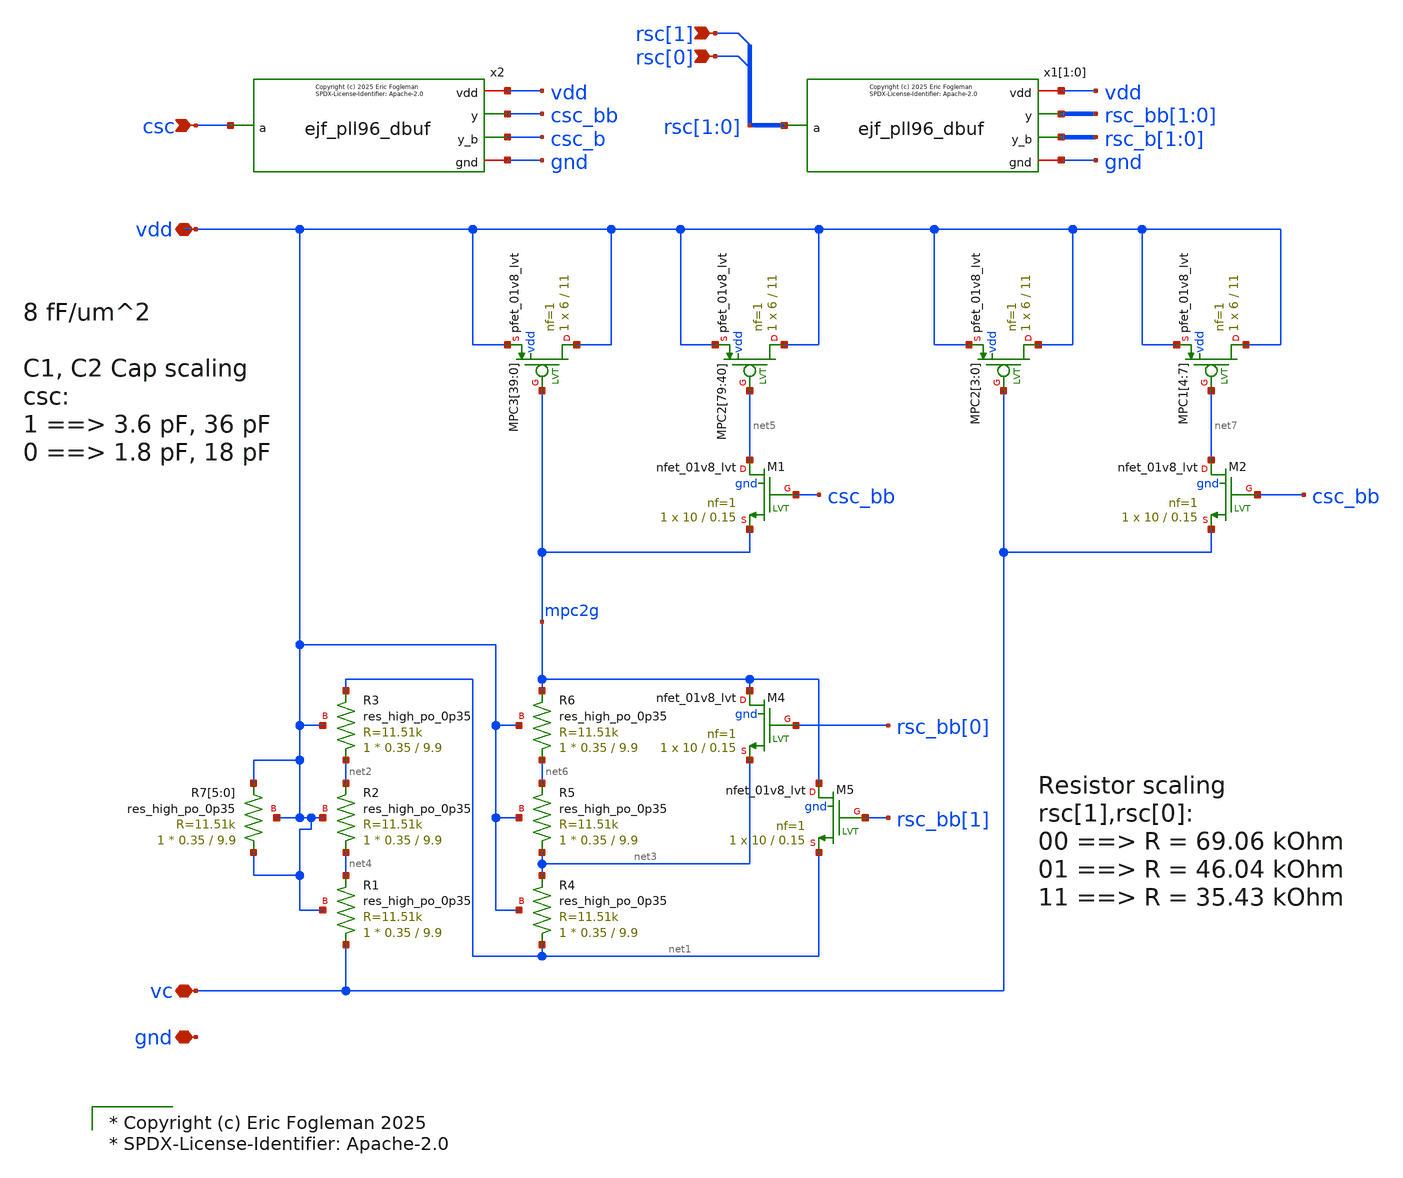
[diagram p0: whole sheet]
** sch_path: xschem/ejf_pll96_lpf.sch
* xschem/ejf_pll96_dbuf.sym:
* Copyright (c) 2025 Eric Fogleman

* Copyright (c) Eric Fogleman 2025
* SPDX-License-Identifier: Apache-2.0

**.subckt ejf_pll96_lpf vc vdd gnd csc rsc[0] rsc[1]
*.iopin vc
*.iopin vdd
*.iopin gnd
*.ipin csc
*.ipin rsc[0]
*.ipin rsc[1]
XMPC2[3] vdd vc vdd vdd sky130_fd_pr__pfet_01v8_lvt L=11 W=6 nf=1 ad='int((nf+1)/2) * W/nf * 0.29' as='int((nf+2)/2) * W/nf * 0.29'
+ pd='2*int((nf+1)/2) * (W/nf + 0.29)' ps='2*int((nf+2)/2) * (W/nf + 0.29)' nrd='0.29 / W' nrs='0.29 / W'
+ sa=0 sb=0 sd=0 mult=1 m=1
XMPC2[2] vdd vc vdd vdd sky130_fd_pr__pfet_01v8_lvt L=11 W=6 nf=1 ad='int((nf+1)/2) * W/nf * 0.29' as='int((nf+2)/2) * W/nf * 0.29'
+ pd='2*int((nf+1)/2) * (W/nf + 0.29)' ps='2*int((nf+2)/2) * (W/nf + 0.29)' nrd='0.29 / W' nrs='0.29 / W'
+ sa=0 sb=0 sd=0 mult=1 m=1
XMPC2[1] vdd vc vdd vdd sky130_fd_pr__pfet_01v8_lvt L=11 W=6 nf=1 ad='int((nf+1)/2) * W/nf * 0.29' as='int((nf+2)/2) * W/nf * 0.29'
+ pd='2*int((nf+1)/2) * (W/nf + 0.29)' ps='2*int((nf+2)/2) * (W/nf + 0.29)' nrd='0.29 / W' nrs='0.29 / W'
+ sa=0 sb=0 sd=0 mult=1 m=1
XMPC2[0] vdd vc vdd vdd sky130_fd_pr__pfet_01v8_lvt L=11 W=6 nf=1 ad='int((nf+1)/2) * W/nf * 0.29' as='int((nf+2)/2) * W/nf * 0.29'
+ pd='2*int((nf+1)/2) * (W/nf + 0.29)' ps='2*int((nf+2)/2) * (W/nf + 0.29)' nrd='0.29 / W' nrs='0.29 / W'
+ sa=0 sb=0 sd=0 mult=1 m=1
XMPC2[79] vdd net5 vdd vdd sky130_fd_pr__pfet_01v8_lvt L=11 W=6 nf=1 ad='int((nf+1)/2) * W/nf * 0.29'
+ as='int((nf+2)/2) * W/nf * 0.29' pd='2*int((nf+1)/2) * (W/nf + 0.29)' ps='2*int((nf+2)/2) * (W/nf + 0.29)'
+ nrd='0.29 / W' nrs='0.29 / W' sa=0 sb=0 sd=0 mult=1 m=1
XMPC2[78] vdd net5 vdd vdd sky130_fd_pr__pfet_01v8_lvt L=11 W=6 nf=1 ad='int((nf+1)/2) * W/nf * 0.29'
+ as='int((nf+2)/2) * W/nf * 0.29' pd='2*int((nf+1)/2) * (W/nf + 0.29)' ps='2*int((nf+2)/2) * (W/nf + 0.29)'
+ nrd='0.29 / W' nrs='0.29 / W' sa=0 sb=0 sd=0 mult=1 m=1
XMPC2[77] vdd net5 vdd vdd sky130_fd_pr__pfet_01v8_lvt L=11 W=6 nf=1 ad='int((nf+1)/2) * W/nf * 0.29'
+ as='int((nf+2)/2) * W/nf * 0.29' pd='2*int((nf+1)/2) * (W/nf + 0.29)' ps='2*int((nf+2)/2) * (W/nf + 0.29)'
+ nrd='0.29 / W' nrs='0.29 / W' sa=0 sb=0 sd=0 mult=1 m=1
XMPC2[76] vdd net5 vdd vdd sky130_fd_pr__pfet_01v8_lvt L=11 W=6 nf=1 ad='int((nf+1)/2) * W/nf * 0.29'
+ as='int((nf+2)/2) * W/nf * 0.29' pd='2*int((nf+1)/2) * (W/nf + 0.29)' ps='2*int((nf+2)/2) * (W/nf + 0.29)'
+ nrd='0.29 / W' nrs='0.29 / W' sa=0 sb=0 sd=0 mult=1 m=1
XMPC2[75] vdd net5 vdd vdd sky130_fd_pr__pfet_01v8_lvt L=11 W=6 nf=1 ad='int((nf+1)/2) * W/nf * 0.29'
+ as='int((nf+2)/2) * W/nf * 0.29' pd='2*int((nf+1)/2) * (W/nf + 0.29)' ps='2*int((nf+2)/2) * (W/nf + 0.29)'
+ nrd='0.29 / W' nrs='0.29 / W' sa=0 sb=0 sd=0 mult=1 m=1
XMPC2[74] vdd net5 vdd vdd sky130_fd_pr__pfet_01v8_lvt L=11 W=6 nf=1 ad='int((nf+1)/2) * W/nf * 0.29'
+ as='int((nf+2)/2) * W/nf * 0.29' pd='2*int((nf+1)/2) * (W/nf + 0.29)' ps='2*int((nf+2)/2) * (W/nf + 0.29)'
+ nrd='0.29 / W' nrs='0.29 / W' sa=0 sb=0 sd=0 mult=1 m=1
XMPC2[73] vdd net5 vdd vdd sky130_fd_pr__pfet_01v8_lvt L=11 W=6 nf=1 ad='int((nf+1)/2) * W/nf * 0.29'
+ as='int((nf+2)/2) * W/nf * 0.29' pd='2*int((nf+1)/2) * (W/nf + 0.29)' ps='2*int((nf+2)/2) * (W/nf + 0.29)'
+ nrd='0.29 / W' nrs='0.29 / W' sa=0 sb=0 sd=0 mult=1 m=1
XMPC2[72] vdd net5 vdd vdd sky130_fd_pr__pfet_01v8_lvt L=11 W=6 nf=1 ad='int((nf+1)/2) * W/nf * 0.29'
+ as='int((nf+2)/2) * W/nf * 0.29' pd='2*int((nf+1)/2) * (W/nf + 0.29)' ps='2*int((nf+2)/2) * (W/nf + 0.29)'
+ nrd='0.29 / W' nrs='0.29 / W' sa=0 sb=0 sd=0 mult=1 m=1
XMPC2[71] vdd net5 vdd vdd sky130_fd_pr__pfet_01v8_lvt L=11 W=6 nf=1 ad='int((nf+1)/2) * W/nf * 0.29'
+ as='int((nf+2)/2) * W/nf * 0.29' pd='2*int((nf+1)/2) * (W/nf + 0.29)' ps='2*int((nf+2)/2) * (W/nf + 0.29)'
+ nrd='0.29 / W' nrs='0.29 / W' sa=0 sb=0 sd=0 mult=1 m=1
XMPC2[70] vdd net5 vdd vdd sky130_fd_pr__pfet_01v8_lvt L=11 W=6 nf=1 ad='int((nf+1)/2) * W/nf * 0.29'
+ as='int((nf+2)/2) * W/nf * 0.29' pd='2*int((nf+1)/2) * (W/nf + 0.29)' ps='2*int((nf+2)/2) * (W/nf + 0.29)'
+ nrd='0.29 / W' nrs='0.29 / W' sa=0 sb=0 sd=0 mult=1 m=1
XMPC2[69] vdd net5 vdd vdd sky130_fd_pr__pfet_01v8_lvt L=11 W=6 nf=1 ad='int((nf+1)/2) * W/nf * 0.29'
+ as='int((nf+2)/2) * W/nf * 0.29' pd='2*int((nf+1)/2) * (W/nf + 0.29)' ps='2*int((nf+2)/2) * (W/nf + 0.29)'
+ nrd='0.29 / W' nrs='0.29 / W' sa=0 sb=0 sd=0 mult=1 m=1
XMPC2[68] vdd net5 vdd vdd sky130_fd_pr__pfet_01v8_lvt L=11 W=6 nf=1 ad='int((nf+1)/2) * W/nf * 0.29'
+ as='int((nf+2)/2) * W/nf * 0.29' pd='2*int((nf+1)/2) * (W/nf + 0.29)' ps='2*int((nf+2)/2) * (W/nf + 0.29)'
+ nrd='0.29 / W' nrs='0.29 / W' sa=0 sb=0 sd=0 mult=1 m=1
XMPC2[67] vdd net5 vdd vdd sky130_fd_pr__pfet_01v8_lvt L=11 W=6 nf=1 ad='int((nf+1)/2) * W/nf * 0.29'
+ as='int((nf+2)/2) * W/nf * 0.29' pd='2*int((nf+1)/2) * (W/nf + 0.29)' ps='2*int((nf+2)/2) * (W/nf + 0.29)'
+ nrd='0.29 / W' nrs='0.29 / W' sa=0 sb=0 sd=0 mult=1 m=1
XMPC2[66] vdd net5 vdd vdd sky130_fd_pr__pfet_01v8_lvt L=11 W=6 nf=1 ad='int((nf+1)/2) * W/nf * 0.29'
+ as='int((nf+2)/2) * W/nf * 0.29' pd='2*int((nf+1)/2) * (W/nf + 0.29)' ps='2*int((nf+2)/2) * (W/nf + 0.29)'
+ nrd='0.29 / W' nrs='0.29 / W' sa=0 sb=0 sd=0 mult=1 m=1
XMPC2[65] vdd net5 vdd vdd sky130_fd_pr__pfet_01v8_lvt L=11 W=6 nf=1 ad='int((nf+1)/2) * W/nf * 0.29'
+ as='int((nf+2)/2) * W/nf * 0.29' pd='2*int((nf+1)/2) * (W/nf + 0.29)' ps='2*int((nf+2)/2) * (W/nf + 0.29)'
+ nrd='0.29 / W' nrs='0.29 / W' sa=0 sb=0 sd=0 mult=1 m=1
XMPC2[64] vdd net5 vdd vdd sky130_fd_pr__pfet_01v8_lvt L=11 W=6 nf=1 ad='int((nf+1)/2) * W/nf * 0.29'
+ as='int((nf+2)/2) * W/nf * 0.29' pd='2*int((nf+1)/2) * (W/nf + 0.29)' ps='2*int((nf+2)/2) * (W/nf + 0.29)'
+ nrd='0.29 / W' nrs='0.29 / W' sa=0 sb=0 sd=0 mult=1 m=1
XMPC2[63] vdd net5 vdd vdd sky130_fd_pr__pfet_01v8_lvt L=11 W=6 nf=1 ad='int((nf+1)/2) * W/nf * 0.29'
+ as='int((nf+2)/2) * W/nf * 0.29' pd='2*int((nf+1)/2) * (W/nf + 0.29)' ps='2*int((nf+2)/2) * (W/nf + 0.29)'
+ nrd='0.29 / W' nrs='0.29 / W' sa=0 sb=0 sd=0 mult=1 m=1
XMPC2[62] vdd net5 vdd vdd sky130_fd_pr__pfet_01v8_lvt L=11 W=6 nf=1 ad='int((nf+1)/2) * W/nf * 0.29'
+ as='int((nf+2)/2) * W/nf * 0.29' pd='2*int((nf+1)/2) * (W/nf + 0.29)' ps='2*int((nf+2)/2) * (W/nf + 0.29)'
+ nrd='0.29 / W' nrs='0.29 / W' sa=0 sb=0 sd=0 mult=1 m=1
XMPC2[61] vdd net5 vdd vdd sky130_fd_pr__pfet_01v8_lvt L=11 W=6 nf=1 ad='int((nf+1)/2) * W/nf * 0.29'
+ as='int((nf+2)/2) * W/nf * 0.29' pd='2*int((nf+1)/2) * (W/nf + 0.29)' ps='2*int((nf+2)/2) * (W/nf + 0.29)'
+ nrd='0.29 / W' nrs='0.29 / W' sa=0 sb=0 sd=0 mult=1 m=1
XMPC2[60] vdd net5 vdd vdd sky130_fd_pr__pfet_01v8_lvt L=11 W=6 nf=1 ad='int((nf+1)/2) * W/nf * 0.29'
+ as='int((nf+2)/2) * W/nf * 0.29' pd='2*int((nf+1)/2) * (W/nf + 0.29)' ps='2*int((nf+2)/2) * (W/nf + 0.29)'
+ nrd='0.29 / W' nrs='0.29 / W' sa=0 sb=0 sd=0 mult=1 m=1
XMPC2[59] vdd net5 vdd vdd sky130_fd_pr__pfet_01v8_lvt L=11 W=6 nf=1 ad='int((nf+1)/2) * W/nf * 0.29'
+ as='int((nf+2)/2) * W/nf * 0.29' pd='2*int((nf+1)/2) * (W/nf + 0.29)' ps='2*int((nf+2)/2) * (W/nf + 0.29)'
+ nrd='0.29 / W' nrs='0.29 / W' sa=0 sb=0 sd=0 mult=1 m=1
XMPC2[58] vdd net5 vdd vdd sky130_fd_pr__pfet_01v8_lvt L=11 W=6 nf=1 ad='int((nf+1)/2) * W/nf * 0.29'
+ as='int((nf+2)/2) * W/nf * 0.29' pd='2*int((nf+1)/2) * (W/nf + 0.29)' ps='2*int((nf+2)/2) * (W/nf + 0.29)'
+ nrd='0.29 / W' nrs='0.29 / W' sa=0 sb=0 sd=0 mult=1 m=1
XMPC2[57] vdd net5 vdd vdd sky130_fd_pr__pfet_01v8_lvt L=11 W=6 nf=1 ad='int((nf+1)/2) * W/nf * 0.29'
+ as='int((nf+2)/2) * W/nf * 0.29' pd='2*int((nf+1)/2) * (W/nf + 0.29)' ps='2*int((nf+2)/2) * (W/nf + 0.29)'
+ nrd='0.29 / W' nrs='0.29 / W' sa=0 sb=0 sd=0 mult=1 m=1
XMPC2[56] vdd net5 vdd vdd sky130_fd_pr__pfet_01v8_lvt L=11 W=6 nf=1 ad='int((nf+1)/2) * W/nf * 0.29'
+ as='int((nf+2)/2) * W/nf * 0.29' pd='2*int((nf+1)/2) * (W/nf + 0.29)' ps='2*int((nf+2)/2) * (W/nf + 0.29)'
+ nrd='0.29 / W' nrs='0.29 / W' sa=0 sb=0 sd=0 mult=1 m=1
XMPC2[55] vdd net5 vdd vdd sky130_fd_pr__pfet_01v8_lvt L=11 W=6 nf=1 ad='int((nf+1)/2) * W/nf * 0.29'
+ as='int((nf+2)/2) * W/nf * 0.29' pd='2*int((nf+1)/2) * (W/nf + 0.29)' ps='2*int((nf+2)/2) * (W/nf + 0.29)'
+ nrd='0.29 / W' nrs='0.29 / W' sa=0 sb=0 sd=0 mult=1 m=1
XMPC2[54] vdd net5 vdd vdd sky130_fd_pr__pfet_01v8_lvt L=11 W=6 nf=1 ad='int((nf+1)/2) * W/nf * 0.29'
+ as='int((nf+2)/2) * W/nf * 0.29' pd='2*int((nf+1)/2) * (W/nf + 0.29)' ps='2*int((nf+2)/2) * (W/nf + 0.29)'
+ nrd='0.29 / W' nrs='0.29 / W' sa=0 sb=0 sd=0 mult=1 m=1
XMPC2[53] vdd net5 vdd vdd sky130_fd_pr__pfet_01v8_lvt L=11 W=6 nf=1 ad='int((nf+1)/2) * W/nf * 0.29'
+ as='int((nf+2)/2) * W/nf * 0.29' pd='2*int((nf+1)/2) * (W/nf + 0.29)' ps='2*int((nf+2)/2) * (W/nf + 0.29)'
+ nrd='0.29 / W' nrs='0.29 / W' sa=0 sb=0 sd=0 mult=1 m=1
XMPC2[52] vdd net5 vdd vdd sky130_fd_pr__pfet_01v8_lvt L=11 W=6 nf=1 ad='int((nf+1)/2) * W/nf * 0.29'
+ as='int((nf+2)/2) * W/nf * 0.29' pd='2*int((nf+1)/2) * (W/nf + 0.29)' ps='2*int((nf+2)/2) * (W/nf + 0.29)'
+ nrd='0.29 / W' nrs='0.29 / W' sa=0 sb=0 sd=0 mult=1 m=1
XMPC2[51] vdd net5 vdd vdd sky130_fd_pr__pfet_01v8_lvt L=11 W=6 nf=1 ad='int((nf+1)/2) * W/nf * 0.29'
+ as='int((nf+2)/2) * W/nf * 0.29' pd='2*int((nf+1)/2) * (W/nf + 0.29)' ps='2*int((nf+2)/2) * (W/nf + 0.29)'
+ nrd='0.29 / W' nrs='0.29 / W' sa=0 sb=0 sd=0 mult=1 m=1
XMPC2[50] vdd net5 vdd vdd sky130_fd_pr__pfet_01v8_lvt L=11 W=6 nf=1 ad='int((nf+1)/2) * W/nf * 0.29'
+ as='int((nf+2)/2) * W/nf * 0.29' pd='2*int((nf+1)/2) * (W/nf + 0.29)' ps='2*int((nf+2)/2) * (W/nf + 0.29)'
+ nrd='0.29 / W' nrs='0.29 / W' sa=0 sb=0 sd=0 mult=1 m=1
XMPC2[49] vdd net5 vdd vdd sky130_fd_pr__pfet_01v8_lvt L=11 W=6 nf=1 ad='int((nf+1)/2) * W/nf * 0.29'
+ as='int((nf+2)/2) * W/nf * 0.29' pd='2*int((nf+1)/2) * (W/nf + 0.29)' ps='2*int((nf+2)/2) * (W/nf + 0.29)'
+ nrd='0.29 / W' nrs='0.29 / W' sa=0 sb=0 sd=0 mult=1 m=1
XMPC2[48] vdd net5 vdd vdd sky130_fd_pr__pfet_01v8_lvt L=11 W=6 nf=1 ad='int((nf+1)/2) * W/nf * 0.29'
+ as='int((nf+2)/2) * W/nf * 0.29' pd='2*int((nf+1)/2) * (W/nf + 0.29)' ps='2*int((nf+2)/2) * (W/nf + 0.29)'
+ nrd='0.29 / W' nrs='0.29 / W' sa=0 sb=0 sd=0 mult=1 m=1
XMPC2[47] vdd net5 vdd vdd sky130_fd_pr__pfet_01v8_lvt L=11 W=6 nf=1 ad='int((nf+1)/2) * W/nf * 0.29'
+ as='int((nf+2)/2) * W/nf * 0.29' pd='2*int((nf+1)/2) * (W/nf + 0.29)' ps='2*int((nf+2)/2) * (W/nf + 0.29)'
+ nrd='0.29 / W' nrs='0.29 / W' sa=0 sb=0 sd=0 mult=1 m=1
XMPC2[46] vdd net5 vdd vdd sky130_fd_pr__pfet_01v8_lvt L=11 W=6 nf=1 ad='int((nf+1)/2) * W/nf * 0.29'
+ as='int((nf+2)/2) * W/nf * 0.29' pd='2*int((nf+1)/2) * (W/nf + 0.29)' ps='2*int((nf+2)/2) * (W/nf + 0.29)'
+ nrd='0.29 / W' nrs='0.29 / W' sa=0 sb=0 sd=0 mult=1 m=1
XMPC2[45] vdd net5 vdd vdd sky130_fd_pr__pfet_01v8_lvt L=11 W=6 nf=1 ad='int((nf+1)/2) * W/nf * 0.29'
+ as='int((nf+2)/2) * W/nf * 0.29' pd='2*int((nf+1)/2) * (W/nf + 0.29)' ps='2*int((nf+2)/2) * (W/nf + 0.29)'
+ nrd='0.29 / W' nrs='0.29 / W' sa=0 sb=0 sd=0 mult=1 m=1
XMPC2[44] vdd net5 vdd vdd sky130_fd_pr__pfet_01v8_lvt L=11 W=6 nf=1 ad='int((nf+1)/2) * W/nf * 0.29'
+ as='int((nf+2)/2) * W/nf * 0.29' pd='2*int((nf+1)/2) * (W/nf + 0.29)' ps='2*int((nf+2)/2) * (W/nf + 0.29)'
+ nrd='0.29 / W' nrs='0.29 / W' sa=0 sb=0 sd=0 mult=1 m=1
XMPC2[43] vdd net5 vdd vdd sky130_fd_pr__pfet_01v8_lvt L=11 W=6 nf=1 ad='int((nf+1)/2) * W/nf * 0.29'
+ as='int((nf+2)/2) * W/nf * 0.29' pd='2*int((nf+1)/2) * (W/nf + 0.29)' ps='2*int((nf+2)/2) * (W/nf + 0.29)'
+ nrd='0.29 / W' nrs='0.29 / W' sa=0 sb=0 sd=0 mult=1 m=1
XMPC2[42] vdd net5 vdd vdd sky130_fd_pr__pfet_01v8_lvt L=11 W=6 nf=1 ad='int((nf+1)/2) * W/nf * 0.29'
+ as='int((nf+2)/2) * W/nf * 0.29' pd='2*int((nf+1)/2) * (W/nf + 0.29)' ps='2*int((nf+2)/2) * (W/nf + 0.29)'
+ nrd='0.29 / W' nrs='0.29 / W' sa=0 sb=0 sd=0 mult=1 m=1
XMPC2[41] vdd net5 vdd vdd sky130_fd_pr__pfet_01v8_lvt L=11 W=6 nf=1 ad='int((nf+1)/2) * W/nf * 0.29'
+ as='int((nf+2)/2) * W/nf * 0.29' pd='2*int((nf+1)/2) * (W/nf + 0.29)' ps='2*int((nf+2)/2) * (W/nf + 0.29)'
+ nrd='0.29 / W' nrs='0.29 / W' sa=0 sb=0 sd=0 mult=1 m=1
XMPC2[40] vdd net5 vdd vdd sky130_fd_pr__pfet_01v8_lvt L=11 W=6 nf=1 ad='int((nf+1)/2) * W/nf * 0.29'
+ as='int((nf+2)/2) * W/nf * 0.29' pd='2*int((nf+1)/2) * (W/nf + 0.29)' ps='2*int((nf+2)/2) * (W/nf + 0.29)'
+ nrd='0.29 / W' nrs='0.29 / W' sa=0 sb=0 sd=0 mult=1 m=1
XR7[5] vdd vdd vdd sky130_fd_pr__res_high_po_0p35 L=9.9 mult=1 m=1
XR7[4] vdd vdd vdd sky130_fd_pr__res_high_po_0p35 L=9.9 mult=1 m=1
XR7[3] vdd vdd vdd sky130_fd_pr__res_high_po_0p35 L=9.9 mult=1 m=1
XR7[2] vdd vdd vdd sky130_fd_pr__res_high_po_0p35 L=9.9 mult=1 m=1
XR7[1] vdd vdd vdd sky130_fd_pr__res_high_po_0p35 L=9.9 mult=1 m=1
XR7[0] vdd vdd vdd sky130_fd_pr__res_high_po_0p35 L=9.9 mult=1 m=1
XMPC1[4] vdd net7 vdd vdd sky130_fd_pr__pfet_01v8_lvt L=11 W=6 nf=1 ad='int((nf+1)/2) * W/nf * 0.29'
+ as='int((nf+2)/2) * W/nf * 0.29' pd='2*int((nf+1)/2) * (W/nf + 0.29)' ps='2*int((nf+2)/2) * (W/nf + 0.29)'
+ nrd='0.29 / W' nrs='0.29 / W' sa=0 sb=0 sd=0 mult=1 m=1
XMPC1[5] vdd net7 vdd vdd sky130_fd_pr__pfet_01v8_lvt L=11 W=6 nf=1 ad='int((nf+1)/2) * W/nf * 0.29'
+ as='int((nf+2)/2) * W/nf * 0.29' pd='2*int((nf+1)/2) * (W/nf + 0.29)' ps='2*int((nf+2)/2) * (W/nf + 0.29)'
+ nrd='0.29 / W' nrs='0.29 / W' sa=0 sb=0 sd=0 mult=1 m=1
XMPC1[6] vdd net7 vdd vdd sky130_fd_pr__pfet_01v8_lvt L=11 W=6 nf=1 ad='int((nf+1)/2) * W/nf * 0.29'
+ as='int((nf+2)/2) * W/nf * 0.29' pd='2*int((nf+1)/2) * (W/nf + 0.29)' ps='2*int((nf+2)/2) * (W/nf + 0.29)'
+ nrd='0.29 / W' nrs='0.29 / W' sa=0 sb=0 sd=0 mult=1 m=1
XMPC1[7] vdd net7 vdd vdd sky130_fd_pr__pfet_01v8_lvt L=11 W=6 nf=1 ad='int((nf+1)/2) * W/nf * 0.29'
+ as='int((nf+2)/2) * W/nf * 0.29' pd='2*int((nf+1)/2) * (W/nf + 0.29)' ps='2*int((nf+2)/2) * (W/nf + 0.29)'
+ nrd='0.29 / W' nrs='0.29 / W' sa=0 sb=0 sd=0 mult=1 m=1
x2 vdd csc csc_bb csc_b gnd ejf_pll96_dbuf
XM1 net5 csc_bb mpc2g gnd sky130_fd_pr__nfet_01v8_lvt L=0.15 W=10 nf=1 ad='int((nf+1)/2) * W/nf * 0.29'
+ as='int((nf+2)/2) * W/nf * 0.29' pd='2*int((nf+1)/2) * (W/nf + 0.29)' ps='2*int((nf+2)/2) * (W/nf + 0.29)'
+ nrd='0.29 / W' nrs='0.29 / W' sa=0 sb=0 sd=0 mult=1 m=1
XM2 net7 csc_bb vc gnd sky130_fd_pr__nfet_01v8_lvt L=0.15 W=10 nf=1 ad='int((nf+1)/2) * W/nf * 0.29'
+ as='int((nf+2)/2) * W/nf * 0.29' pd='2*int((nf+1)/2) * (W/nf + 0.29)' ps='2*int((nf+2)/2) * (W/nf + 0.29)'
+ nrd='0.29 / W' nrs='0.29 / W' sa=0 sb=0 sd=0 mult=1 m=1
XR1 vc net4 vdd sky130_fd_pr__res_high_po_0p35 L=9.9 mult=1 m=1
XR2 net4 net2 vdd sky130_fd_pr__res_high_po_0p35 L=9.9 mult=1 m=1
XR3 net2 net1 vdd sky130_fd_pr__res_high_po_0p35 L=9.9 mult=1 m=1
XR4 net1 net3 vdd sky130_fd_pr__res_high_po_0p35 L=9.9 mult=1 m=1
XR5 net3 net6 vdd sky130_fd_pr__res_high_po_0p35 L=9.9 mult=1 m=1
XR6 net6 mpc2g vdd sky130_fd_pr__res_high_po_0p35 L=9.9 mult=1 m=1
XM4 mpc2g rsc_bb[0] net3 gnd sky130_fd_pr__nfet_01v8_lvt L=0.15 W=10 nf=1 ad='int((nf+1)/2) * W/nf * 0.29'
+ as='int((nf+2)/2) * W/nf * 0.29' pd='2*int((nf+1)/2) * (W/nf + 0.29)' ps='2*int((nf+2)/2) * (W/nf + 0.29)'
+ nrd='0.29 / W' nrs='0.29 / W' sa=0 sb=0 sd=0 mult=1 m=1
XM5 mpc2g rsc_bb[1] net1 gnd sky130_fd_pr__nfet_01v8_lvt L=0.15 W=10 nf=1 ad='int((nf+1)/2) * W/nf * 0.29'
+ as='int((nf+2)/2) * W/nf * 0.29' pd='2*int((nf+1)/2) * (W/nf + 0.29)' ps='2*int((nf+2)/2) * (W/nf + 0.29)'
+ nrd='0.29 / W' nrs='0.29 / W' sa=0 sb=0 sd=0 mult=1 m=1
x1[1] vdd rsc[1] rsc_bb[1] rsc_b[1] gnd ejf_pll96_dbuf
x1[0] vdd rsc[0] rsc_bb[0] rsc_b[0] gnd ejf_pll96_dbuf
XMPC3[39] vdd mpc2g vdd vdd sky130_fd_pr__pfet_01v8_lvt L=11 W=6 nf=1 ad='int((nf+1)/2) * W/nf * 0.29'
+ as='int((nf+2)/2) * W/nf * 0.29' pd='2*int((nf+1)/2) * (W/nf + 0.29)' ps='2*int((nf+2)/2) * (W/nf + 0.29)'
+ nrd='0.29 / W' nrs='0.29 / W' sa=0 sb=0 sd=0 mult=1 m=1
XMPC3[38] vdd mpc2g vdd vdd sky130_fd_pr__pfet_01v8_lvt L=11 W=6 nf=1 ad='int((nf+1)/2) * W/nf * 0.29'
+ as='int((nf+2)/2) * W/nf * 0.29' pd='2*int((nf+1)/2) * (W/nf + 0.29)' ps='2*int((nf+2)/2) * (W/nf + 0.29)'
+ nrd='0.29 / W' nrs='0.29 / W' sa=0 sb=0 sd=0 mult=1 m=1
XMPC3[37] vdd mpc2g vdd vdd sky130_fd_pr__pfet_01v8_lvt L=11 W=6 nf=1 ad='int((nf+1)/2) * W/nf * 0.29'
+ as='int((nf+2)/2) * W/nf * 0.29' pd='2*int((nf+1)/2) * (W/nf + 0.29)' ps='2*int((nf+2)/2) * (W/nf + 0.29)'
+ nrd='0.29 / W' nrs='0.29 / W' sa=0 sb=0 sd=0 mult=1 m=1
XMPC3[36] vdd mpc2g vdd vdd sky130_fd_pr__pfet_01v8_lvt L=11 W=6 nf=1 ad='int((nf+1)/2) * W/nf * 0.29'
+ as='int((nf+2)/2) * W/nf * 0.29' pd='2*int((nf+1)/2) * (W/nf + 0.29)' ps='2*int((nf+2)/2) * (W/nf + 0.29)'
+ nrd='0.29 / W' nrs='0.29 / W' sa=0 sb=0 sd=0 mult=1 m=1
XMPC3[35] vdd mpc2g vdd vdd sky130_fd_pr__pfet_01v8_lvt L=11 W=6 nf=1 ad='int((nf+1)/2) * W/nf * 0.29'
+ as='int((nf+2)/2) * W/nf * 0.29' pd='2*int((nf+1)/2) * (W/nf + 0.29)' ps='2*int((nf+2)/2) * (W/nf + 0.29)'
+ nrd='0.29 / W' nrs='0.29 / W' sa=0 sb=0 sd=0 mult=1 m=1
XMPC3[34] vdd mpc2g vdd vdd sky130_fd_pr__pfet_01v8_lvt L=11 W=6 nf=1 ad='int((nf+1)/2) * W/nf * 0.29'
+ as='int((nf+2)/2) * W/nf * 0.29' pd='2*int((nf+1)/2) * (W/nf + 0.29)' ps='2*int((nf+2)/2) * (W/nf + 0.29)'
+ nrd='0.29 / W' nrs='0.29 / W' sa=0 sb=0 sd=0 mult=1 m=1
XMPC3[33] vdd mpc2g vdd vdd sky130_fd_pr__pfet_01v8_lvt L=11 W=6 nf=1 ad='int((nf+1)/2) * W/nf * 0.29'
+ as='int((nf+2)/2) * W/nf * 0.29' pd='2*int((nf+1)/2) * (W/nf + 0.29)' ps='2*int((nf+2)/2) * (W/nf + 0.29)'
+ nrd='0.29 / W' nrs='0.29 / W' sa=0 sb=0 sd=0 mult=1 m=1
XMPC3[32] vdd mpc2g vdd vdd sky130_fd_pr__pfet_01v8_lvt L=11 W=6 nf=1 ad='int((nf+1)/2) * W/nf * 0.29'
+ as='int((nf+2)/2) * W/nf * 0.29' pd='2*int((nf+1)/2) * (W/nf + 0.29)' ps='2*int((nf+2)/2) * (W/nf + 0.29)'
+ nrd='0.29 / W' nrs='0.29 / W' sa=0 sb=0 sd=0 mult=1 m=1
XMPC3[31] vdd mpc2g vdd vdd sky130_fd_pr__pfet_01v8_lvt L=11 W=6 nf=1 ad='int((nf+1)/2) * W/nf * 0.29'
+ as='int((nf+2)/2) * W/nf * 0.29' pd='2*int((nf+1)/2) * (W/nf + 0.29)' ps='2*int((nf+2)/2) * (W/nf + 0.29)'
+ nrd='0.29 / W' nrs='0.29 / W' sa=0 sb=0 sd=0 mult=1 m=1
XMPC3[30] vdd mpc2g vdd vdd sky130_fd_pr__pfet_01v8_lvt L=11 W=6 nf=1 ad='int((nf+1)/2) * W/nf * 0.29'
+ as='int((nf+2)/2) * W/nf * 0.29' pd='2*int((nf+1)/2) * (W/nf + 0.29)' ps='2*int((nf+2)/2) * (W/nf + 0.29)'
+ nrd='0.29 / W' nrs='0.29 / W' sa=0 sb=0 sd=0 mult=1 m=1
XMPC3[29] vdd mpc2g vdd vdd sky130_fd_pr__pfet_01v8_lvt L=11 W=6 nf=1 ad='int((nf+1)/2) * W/nf * 0.29'
+ as='int((nf+2)/2) * W/nf * 0.29' pd='2*int((nf+1)/2) * (W/nf + 0.29)' ps='2*int((nf+2)/2) * (W/nf + 0.29)'
+ nrd='0.29 / W' nrs='0.29 / W' sa=0 sb=0 sd=0 mult=1 m=1
XMPC3[28] vdd mpc2g vdd vdd sky130_fd_pr__pfet_01v8_lvt L=11 W=6 nf=1 ad='int((nf+1)/2) * W/nf * 0.29'
+ as='int((nf+2)/2) * W/nf * 0.29' pd='2*int((nf+1)/2) * (W/nf + 0.29)' ps='2*int((nf+2)/2) * (W/nf + 0.29)'
+ nrd='0.29 / W' nrs='0.29 / W' sa=0 sb=0 sd=0 mult=1 m=1
XMPC3[27] vdd mpc2g vdd vdd sky130_fd_pr__pfet_01v8_lvt L=11 W=6 nf=1 ad='int((nf+1)/2) * W/nf * 0.29'
+ as='int((nf+2)/2) * W/nf * 0.29' pd='2*int((nf+1)/2) * (W/nf + 0.29)' ps='2*int((nf+2)/2) * (W/nf + 0.29)'
+ nrd='0.29 / W' nrs='0.29 / W' sa=0 sb=0 sd=0 mult=1 m=1
XMPC3[26] vdd mpc2g vdd vdd sky130_fd_pr__pfet_01v8_lvt L=11 W=6 nf=1 ad='int((nf+1)/2) * W/nf * 0.29'
+ as='int((nf+2)/2) * W/nf * 0.29' pd='2*int((nf+1)/2) * (W/nf + 0.29)' ps='2*int((nf+2)/2) * (W/nf + 0.29)'
+ nrd='0.29 / W' nrs='0.29 / W' sa=0 sb=0 sd=0 mult=1 m=1
XMPC3[25] vdd mpc2g vdd vdd sky130_fd_pr__pfet_01v8_lvt L=11 W=6 nf=1 ad='int((nf+1)/2) * W/nf * 0.29'
+ as='int((nf+2)/2) * W/nf * 0.29' pd='2*int((nf+1)/2) * (W/nf + 0.29)' ps='2*int((nf+2)/2) * (W/nf + 0.29)'
+ nrd='0.29 / W' nrs='0.29 / W' sa=0 sb=0 sd=0 mult=1 m=1
XMPC3[24] vdd mpc2g vdd vdd sky130_fd_pr__pfet_01v8_lvt L=11 W=6 nf=1 ad='int((nf+1)/2) * W/nf * 0.29'
+ as='int((nf+2)/2) * W/nf * 0.29' pd='2*int((nf+1)/2) * (W/nf + 0.29)' ps='2*int((nf+2)/2) * (W/nf + 0.29)'
+ nrd='0.29 / W' nrs='0.29 / W' sa=0 sb=0 sd=0 mult=1 m=1
XMPC3[23] vdd mpc2g vdd vdd sky130_fd_pr__pfet_01v8_lvt L=11 W=6 nf=1 ad='int((nf+1)/2) * W/nf * 0.29'
+ as='int((nf+2)/2) * W/nf * 0.29' pd='2*int((nf+1)/2) * (W/nf + 0.29)' ps='2*int((nf+2)/2) * (W/nf + 0.29)'
+ nrd='0.29 / W' nrs='0.29 / W' sa=0 sb=0 sd=0 mult=1 m=1
XMPC3[22] vdd mpc2g vdd vdd sky130_fd_pr__pfet_01v8_lvt L=11 W=6 nf=1 ad='int((nf+1)/2) * W/nf * 0.29'
+ as='int((nf+2)/2) * W/nf * 0.29' pd='2*int((nf+1)/2) * (W/nf + 0.29)' ps='2*int((nf+2)/2) * (W/nf + 0.29)'
+ nrd='0.29 / W' nrs='0.29 / W' sa=0 sb=0 sd=0 mult=1 m=1
XMPC3[21] vdd mpc2g vdd vdd sky130_fd_pr__pfet_01v8_lvt L=11 W=6 nf=1 ad='int((nf+1)/2) * W/nf * 0.29'
+ as='int((nf+2)/2) * W/nf * 0.29' pd='2*int((nf+1)/2) * (W/nf + 0.29)' ps='2*int((nf+2)/2) * (W/nf + 0.29)'
+ nrd='0.29 / W' nrs='0.29 / W' sa=0 sb=0 sd=0 mult=1 m=1
XMPC3[20] vdd mpc2g vdd vdd sky130_fd_pr__pfet_01v8_lvt L=11 W=6 nf=1 ad='int((nf+1)/2) * W/nf * 0.29'
+ as='int((nf+2)/2) * W/nf * 0.29' pd='2*int((nf+1)/2) * (W/nf + 0.29)' ps='2*int((nf+2)/2) * (W/nf + 0.29)'
+ nrd='0.29 / W' nrs='0.29 / W' sa=0 sb=0 sd=0 mult=1 m=1
XMPC3[19] vdd mpc2g vdd vdd sky130_fd_pr__pfet_01v8_lvt L=11 W=6 nf=1 ad='int((nf+1)/2) * W/nf * 0.29'
+ as='int((nf+2)/2) * W/nf * 0.29' pd='2*int((nf+1)/2) * (W/nf + 0.29)' ps='2*int((nf+2)/2) * (W/nf + 0.29)'
+ nrd='0.29 / W' nrs='0.29 / W' sa=0 sb=0 sd=0 mult=1 m=1
XMPC3[18] vdd mpc2g vdd vdd sky130_fd_pr__pfet_01v8_lvt L=11 W=6 nf=1 ad='int((nf+1)/2) * W/nf * 0.29'
+ as='int((nf+2)/2) * W/nf * 0.29' pd='2*int((nf+1)/2) * (W/nf + 0.29)' ps='2*int((nf+2)/2) * (W/nf + 0.29)'
+ nrd='0.29 / W' nrs='0.29 / W' sa=0 sb=0 sd=0 mult=1 m=1
XMPC3[17] vdd mpc2g vdd vdd sky130_fd_pr__pfet_01v8_lvt L=11 W=6 nf=1 ad='int((nf+1)/2) * W/nf * 0.29'
+ as='int((nf+2)/2) * W/nf * 0.29' pd='2*int((nf+1)/2) * (W/nf + 0.29)' ps='2*int((nf+2)/2) * (W/nf + 0.29)'
+ nrd='0.29 / W' nrs='0.29 / W' sa=0 sb=0 sd=0 mult=1 m=1
XMPC3[16] vdd mpc2g vdd vdd sky130_fd_pr__pfet_01v8_lvt L=11 W=6 nf=1 ad='int((nf+1)/2) * W/nf * 0.29'
+ as='int((nf+2)/2) * W/nf * 0.29' pd='2*int((nf+1)/2) * (W/nf + 0.29)' ps='2*int((nf+2)/2) * (W/nf + 0.29)'
+ nrd='0.29 / W' nrs='0.29 / W' sa=0 sb=0 sd=0 mult=1 m=1
XMPC3[15] vdd mpc2g vdd vdd sky130_fd_pr__pfet_01v8_lvt L=11 W=6 nf=1 ad='int((nf+1)/2) * W/nf * 0.29'
+ as='int((nf+2)/2) * W/nf * 0.29' pd='2*int((nf+1)/2) * (W/nf + 0.29)' ps='2*int((nf+2)/2) * (W/nf + 0.29)'
+ nrd='0.29 / W' nrs='0.29 / W' sa=0 sb=0 sd=0 mult=1 m=1
XMPC3[14] vdd mpc2g vdd vdd sky130_fd_pr__pfet_01v8_lvt L=11 W=6 nf=1 ad='int((nf+1)/2) * W/nf * 0.29'
+ as='int((nf+2)/2) * W/nf * 0.29' pd='2*int((nf+1)/2) * (W/nf + 0.29)' ps='2*int((nf+2)/2) * (W/nf + 0.29)'
+ nrd='0.29 / W' nrs='0.29 / W' sa=0 sb=0 sd=0 mult=1 m=1
XMPC3[13] vdd mpc2g vdd vdd sky130_fd_pr__pfet_01v8_lvt L=11 W=6 nf=1 ad='int((nf+1)/2) * W/nf * 0.29'
+ as='int((nf+2)/2) * W/nf * 0.29' pd='2*int((nf+1)/2) * (W/nf + 0.29)' ps='2*int((nf+2)/2) * (W/nf + 0.29)'
+ nrd='0.29 / W' nrs='0.29 / W' sa=0 sb=0 sd=0 mult=1 m=1
XMPC3[12] vdd mpc2g vdd vdd sky130_fd_pr__pfet_01v8_lvt L=11 W=6 nf=1 ad='int((nf+1)/2) * W/nf * 0.29'
+ as='int((nf+2)/2) * W/nf * 0.29' pd='2*int((nf+1)/2) * (W/nf + 0.29)' ps='2*int((nf+2)/2) * (W/nf + 0.29)'
+ nrd='0.29 / W' nrs='0.29 / W' sa=0 sb=0 sd=0 mult=1 m=1
XMPC3[11] vdd mpc2g vdd vdd sky130_fd_pr__pfet_01v8_lvt L=11 W=6 nf=1 ad='int((nf+1)/2) * W/nf * 0.29'
+ as='int((nf+2)/2) * W/nf * 0.29' pd='2*int((nf+1)/2) * (W/nf + 0.29)' ps='2*int((nf+2)/2) * (W/nf + 0.29)'
+ nrd='0.29 / W' nrs='0.29 / W' sa=0 sb=0 sd=0 mult=1 m=1
XMPC3[10] vdd mpc2g vdd vdd sky130_fd_pr__pfet_01v8_lvt L=11 W=6 nf=1 ad='int((nf+1)/2) * W/nf * 0.29'
+ as='int((nf+2)/2) * W/nf * 0.29' pd='2*int((nf+1)/2) * (W/nf + 0.29)' ps='2*int((nf+2)/2) * (W/nf + 0.29)'
+ nrd='0.29 / W' nrs='0.29 / W' sa=0 sb=0 sd=0 mult=1 m=1
XMPC3[9] vdd mpc2g vdd vdd sky130_fd_pr__pfet_01v8_lvt L=11 W=6 nf=1 ad='int((nf+1)/2) * W/nf * 0.29'
+ as='int((nf+2)/2) * W/nf * 0.29' pd='2*int((nf+1)/2) * (W/nf + 0.29)' ps='2*int((nf+2)/2) * (W/nf + 0.29)'
+ nrd='0.29 / W' nrs='0.29 / W' sa=0 sb=0 sd=0 mult=1 m=1
XMPC3[8] vdd mpc2g vdd vdd sky130_fd_pr__pfet_01v8_lvt L=11 W=6 nf=1 ad='int((nf+1)/2) * W/nf * 0.29'
+ as='int((nf+2)/2) * W/nf * 0.29' pd='2*int((nf+1)/2) * (W/nf + 0.29)' ps='2*int((nf+2)/2) * (W/nf + 0.29)'
+ nrd='0.29 / W' nrs='0.29 / W' sa=0 sb=0 sd=0 mult=1 m=1
XMPC3[7] vdd mpc2g vdd vdd sky130_fd_pr__pfet_01v8_lvt L=11 W=6 nf=1 ad='int((nf+1)/2) * W/nf * 0.29'
+ as='int((nf+2)/2) * W/nf * 0.29' pd='2*int((nf+1)/2) * (W/nf + 0.29)' ps='2*int((nf+2)/2) * (W/nf + 0.29)'
+ nrd='0.29 / W' nrs='0.29 / W' sa=0 sb=0 sd=0 mult=1 m=1
XMPC3[6] vdd mpc2g vdd vdd sky130_fd_pr__pfet_01v8_lvt L=11 W=6 nf=1 ad='int((nf+1)/2) * W/nf * 0.29'
+ as='int((nf+2)/2) * W/nf * 0.29' pd='2*int((nf+1)/2) * (W/nf + 0.29)' ps='2*int((nf+2)/2) * (W/nf + 0.29)'
+ nrd='0.29 / W' nrs='0.29 / W' sa=0 sb=0 sd=0 mult=1 m=1
XMPC3[5] vdd mpc2g vdd vdd sky130_fd_pr__pfet_01v8_lvt L=11 W=6 nf=1 ad='int((nf+1)/2) * W/nf * 0.29'
+ as='int((nf+2)/2) * W/nf * 0.29' pd='2*int((nf+1)/2) * (W/nf + 0.29)' ps='2*int((nf+2)/2) * (W/nf + 0.29)'
+ nrd='0.29 / W' nrs='0.29 / W' sa=0 sb=0 sd=0 mult=1 m=1
XMPC3[4] vdd mpc2g vdd vdd sky130_fd_pr__pfet_01v8_lvt L=11 W=6 nf=1 ad='int((nf+1)/2) * W/nf * 0.29'
+ as='int((nf+2)/2) * W/nf * 0.29' pd='2*int((nf+1)/2) * (W/nf + 0.29)' ps='2*int((nf+2)/2) * (W/nf + 0.29)'
+ nrd='0.29 / W' nrs='0.29 / W' sa=0 sb=0 sd=0 mult=1 m=1
XMPC3[3] vdd mpc2g vdd vdd sky130_fd_pr__pfet_01v8_lvt L=11 W=6 nf=1 ad='int((nf+1)/2) * W/nf * 0.29'
+ as='int((nf+2)/2) * W/nf * 0.29' pd='2*int((nf+1)/2) * (W/nf + 0.29)' ps='2*int((nf+2)/2) * (W/nf + 0.29)'
+ nrd='0.29 / W' nrs='0.29 / W' sa=0 sb=0 sd=0 mult=1 m=1
XMPC3[2] vdd mpc2g vdd vdd sky130_fd_pr__pfet_01v8_lvt L=11 W=6 nf=1 ad='int((nf+1)/2) * W/nf * 0.29'
+ as='int((nf+2)/2) * W/nf * 0.29' pd='2*int((nf+1)/2) * (W/nf + 0.29)' ps='2*int((nf+2)/2) * (W/nf + 0.29)'
+ nrd='0.29 / W' nrs='0.29 / W' sa=0 sb=0 sd=0 mult=1 m=1
XMPC3[1] vdd mpc2g vdd vdd sky130_fd_pr__pfet_01v8_lvt L=11 W=6 nf=1 ad='int((nf+1)/2) * W/nf * 0.29'
+ as='int((nf+2)/2) * W/nf * 0.29' pd='2*int((nf+1)/2) * (W/nf + 0.29)' ps='2*int((nf+2)/2) * (W/nf + 0.29)'
+ nrd='0.29 / W' nrs='0.29 / W' sa=0 sb=0 sd=0 mult=1 m=1
XMPC3[0] vdd mpc2g vdd vdd sky130_fd_pr__pfet_01v8_lvt L=11 W=6 nf=1 ad='int((nf+1)/2) * W/nf * 0.29'
+ as='int((nf+2)/2) * W/nf * 0.29' pd='2*int((nf+1)/2) * (W/nf + 0.29)' ps='2*int((nf+2)/2) * (W/nf + 0.29)'
+ nrd='0.29 / W' nrs='0.29 / W' sa=0 sb=0 sd=0 mult=1 m=1
**.ends

* expanding   symbol:  ejf_pll96_dbuf.sym # of pins=5
** sym_path: xschem/ejf_pll96_dbuf.sym
** sch_path: xschem/ejf_pll96_dbuf.sch
.subckt ejf_pll96_dbuf vdd a y y_b gnd
*.ipin a
*.iopin vdd
*.iopin gnd
*.opin y
*.opin y_b
XMP1 y_b a vdd vdd sky130_fd_pr__pfet_01v8_hvt L=0.15 W=1.2 nf=1 ad='int((nf+1)/2) * W/nf * 0.29' as='int((nf+2)/2) * W/nf * 0.29'
+ pd='2*int((nf+1)/2) * (W/nf + 0.29)' ps='2*int((nf+2)/2) * (W/nf + 0.29)' nrd='0.29 / W' nrs='0.29 / W'
+ sa=0 sb=0 sd=0 mult=1 m=1
XMP3 y y_b vdd vdd sky130_fd_pr__pfet_01v8_hvt L=0.15 W=1.2 nf=1 ad='int((nf+1)/2) * W/nf * 0.29' as='int((nf+2)/2) * W/nf * 0.29'
+ pd='2*int((nf+1)/2) * (W/nf + 0.29)' ps='2*int((nf+2)/2) * (W/nf + 0.29)' nrd='0.29 / W' nrs='0.29 / W'
+ sa=0 sb=0 sd=0 mult=1 m=1
XMN4 y y_b gnd gnd sky130_fd_pr__nfet_01v8 L=0.15 W=0.74 nf=1 ad='int((nf+1)/2) * W/nf * 0.29' as='int((nf+2)/2) * W/nf * 0.29'
+ pd='2*int((nf+1)/2) * (W/nf + 0.29)' ps='2*int((nf+2)/2) * (W/nf + 0.29)' nrd='0.29 / W' nrs='0.29 / W'
+ sa=0 sb=0 sd=0 mult=1 m=1
XMN2 y_b a gnd gnd sky130_fd_pr__nfet_01v8 L=0.15 W=0.74 nf=1 ad='int((nf+1)/2) * W/nf * 0.29' as='int((nf+2)/2) * W/nf * 0.29'
+ pd='2*int((nf+1)/2) * (W/nf + 0.29)' ps='2*int((nf+2)/2) * (W/nf + 0.29)' nrd='0.29 / W' nrs='0.29 / W'
+ sa=0 sb=0 sd=0 mult=1 m=1
**** begin user architecture code

* Copyright (c) Eric Fogleman 2025
* SPDX-License-Identifier: Apache-2.0

**** end user architecture code
.ends

.end
